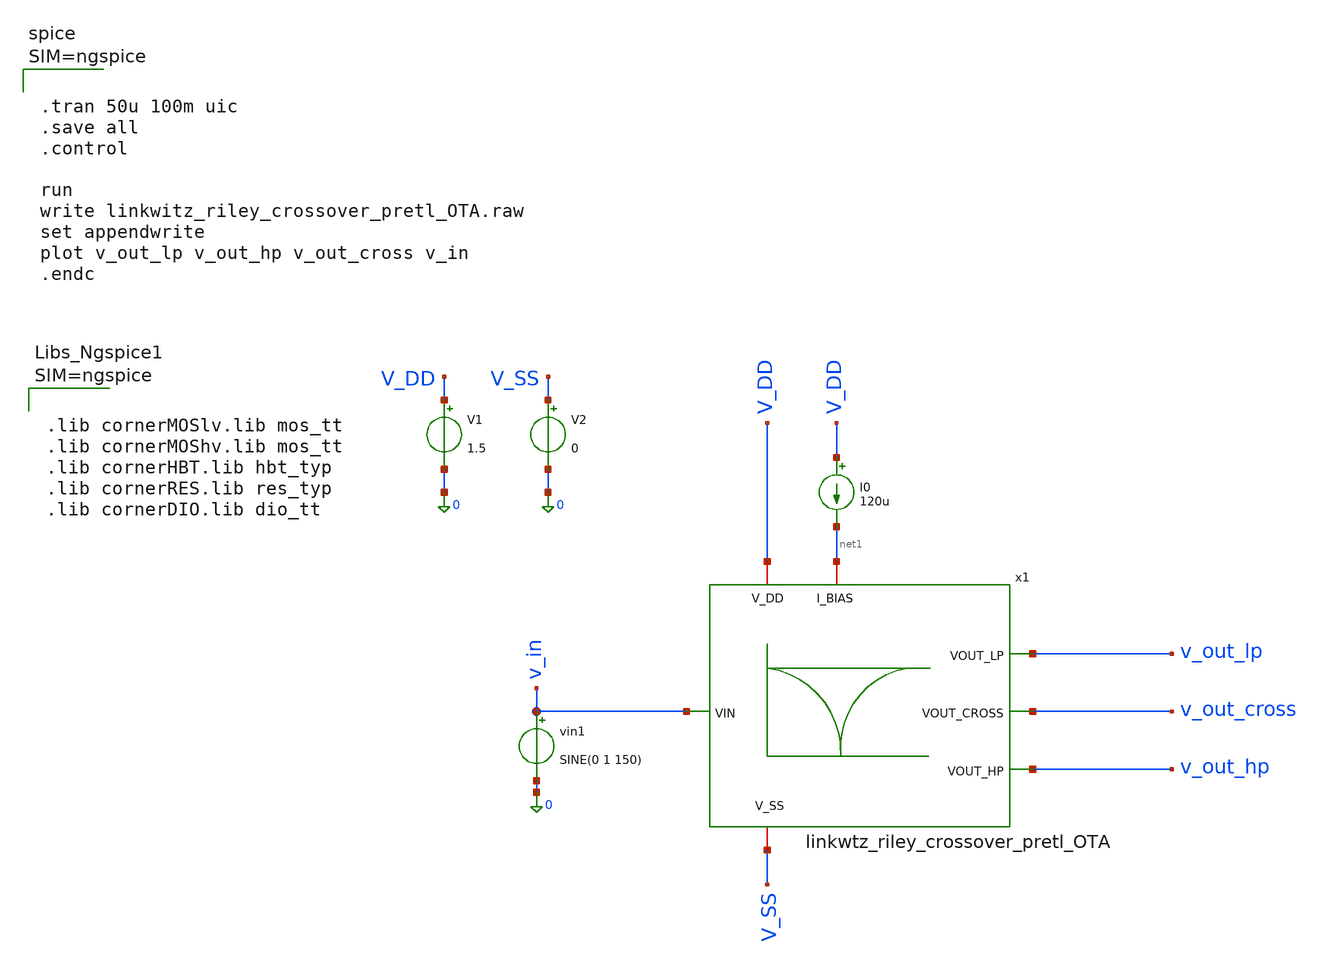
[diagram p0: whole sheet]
** sch_path: 004_Real_Circuits/003_version_second_output_stage/linkwitz_riley_real_circuit_pretl_top_tb_tran.sch
**.subckt linkwitz_riley_real_circuit_pretl_top_tb_tran
I0 V_DD net1 120u
V1 V_DD 0 1.5
vin1 v_in 0 SINE(0 1 150)
V2 V_SS 0 0
x1 v_out_lp net1 V_DD v_out_cross V_SS v_in v_out_hp linkwtz_riley_crossover_pretl_OTA
**** begin user architecture code



.lib cornerMOSlv.lib mos_tt
.lib cornerMOShv.lib mos_tt
.lib cornerHBT.lib hbt_typ
.lib cornerRES.lib res_typ
.lib cornerDIO.lib dio_tt






.tran 50u 100m uic
.save all
.control

run
write linkwitz_riley_crossover_pretl_OTA.raw
set appendwrite
plot v_out_lp v_out_hp v_out_cross v_in
.endc



**** end user architecture code
**.ends
.end
